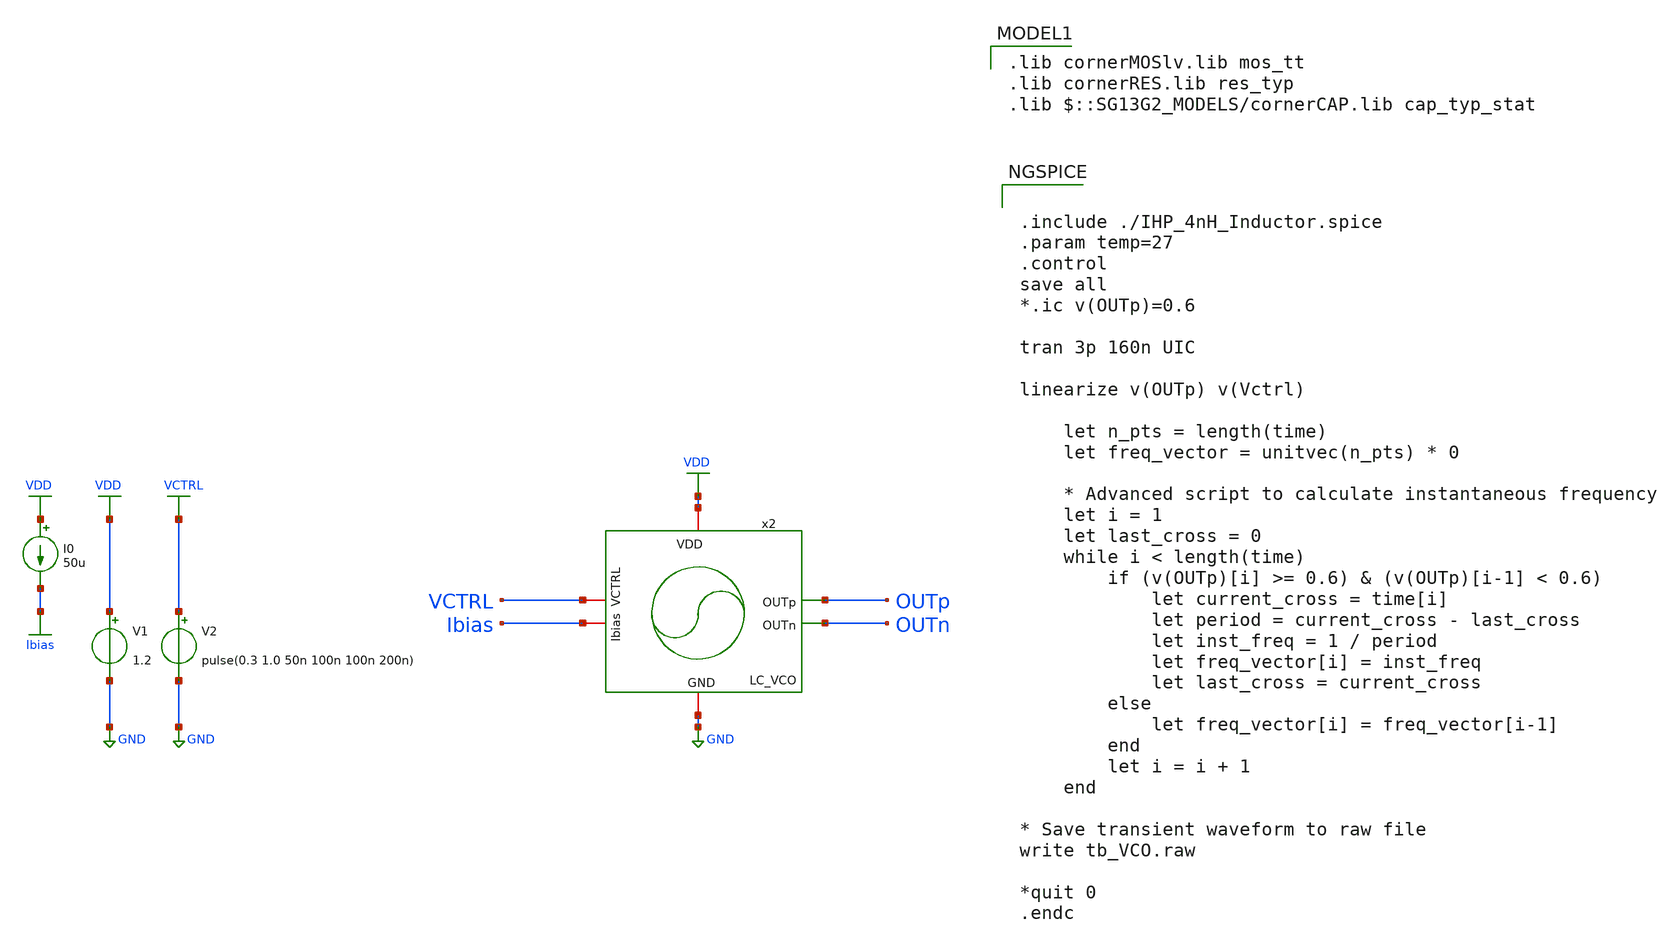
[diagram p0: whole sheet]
** sch_path: schematic/blocks/lc-vco/LC_VCO_sweep_tb.sch
**.subckt LC_VCO_sweep_tb
V2 VCTRL GND pulse(0.3 1.0 50n 100n 100n 200n)
x2 VDD OUTp OUTn Ibias VCTRL GND LC_VCO
V1 VDD GND 1.2
I0 VDD Ibias 50u
**** begin user architecture code


.include ./IHP_4nH_Inductor.spice
.param temp=27
.control
save all
*.ic v(OUTp)=0.6

tran 3p 160n UIC

linearize v(OUTp) v(Vctrl)

    let n_pts = length(time)
    let freq_vector = unitvec(n_pts) * 0

    * Advanced script to calculate instantaneous frequency
    let i = 1
    let last_cross = 0
    while i < length(time)
        if (v(OUTp)[i] >= 0.6) & (v(OUTp)[i-1] < 0.6)
            let current_cross = time[i]
            let period = current_cross - last_cross
            let inst_freq = 1 / period
            let freq_vector[i] = inst_freq
            let last_cross = current_cross
        else
            let freq_vector[i] = freq_vector[i-1]
        end
        let i = i + 1
    end

* Save transient waveform to raw file
write tb_VCO.raw

*quit 0
.endc


 .lib cornerMOSlv.lib mos_tt
.lib cornerRES.lib res_typ
.lib $::SG13G2_MODELS/cornerCAP.lib cap_typ_stat

**** end user architecture code
**.ends
.GLOBAL GND
.GLOBAL VCTRL
.GLOBAL VDD
.GLOBAL Ibias
.end
